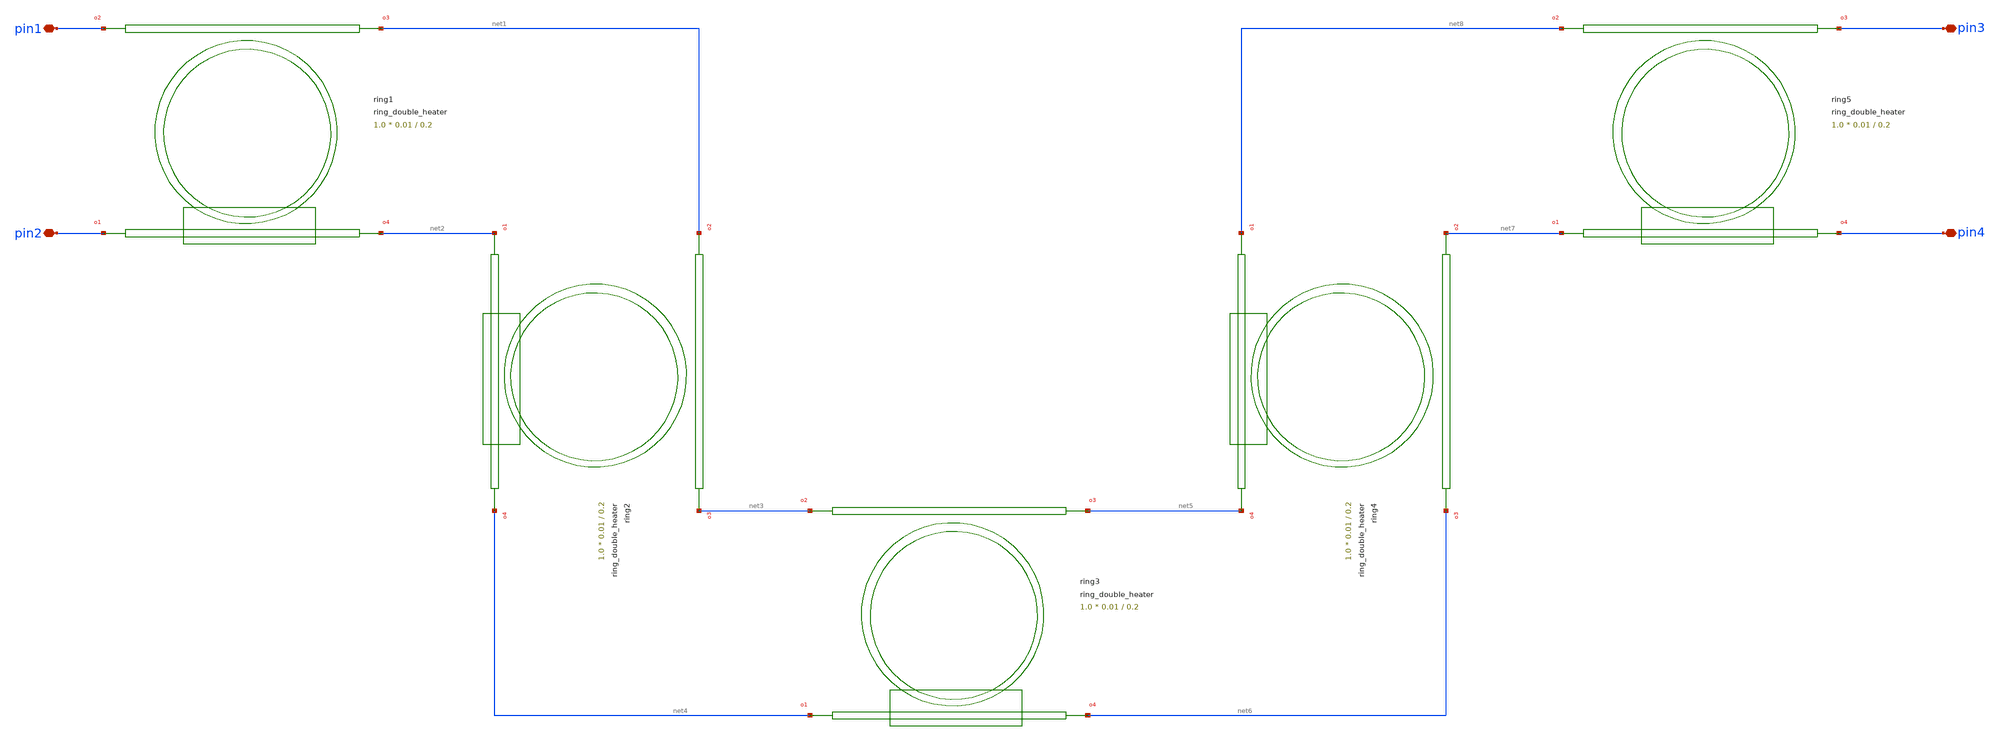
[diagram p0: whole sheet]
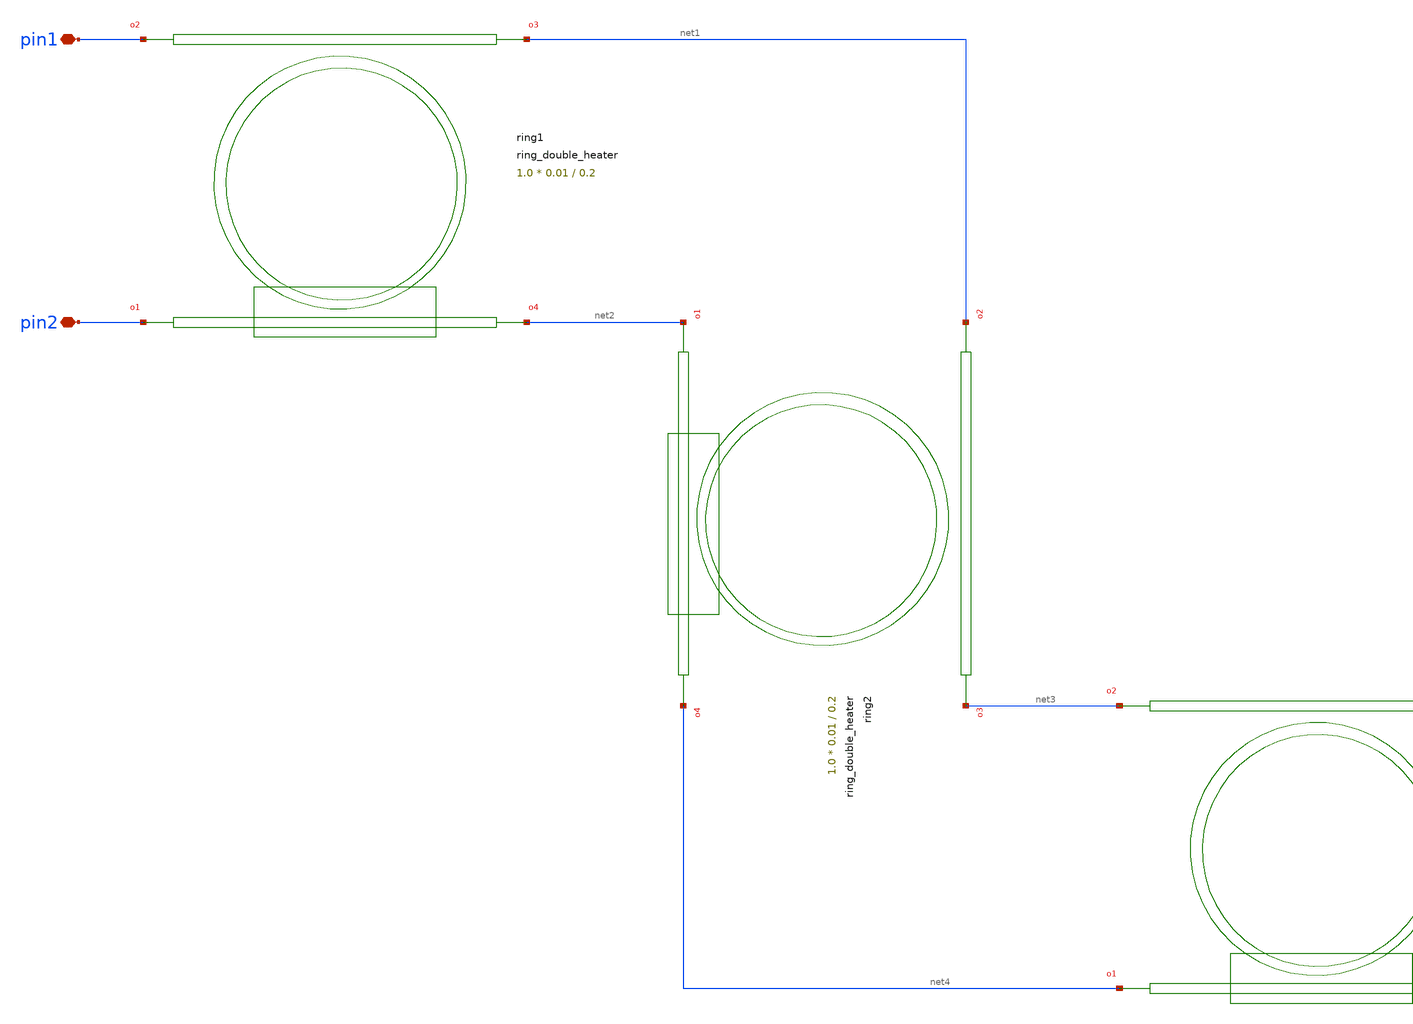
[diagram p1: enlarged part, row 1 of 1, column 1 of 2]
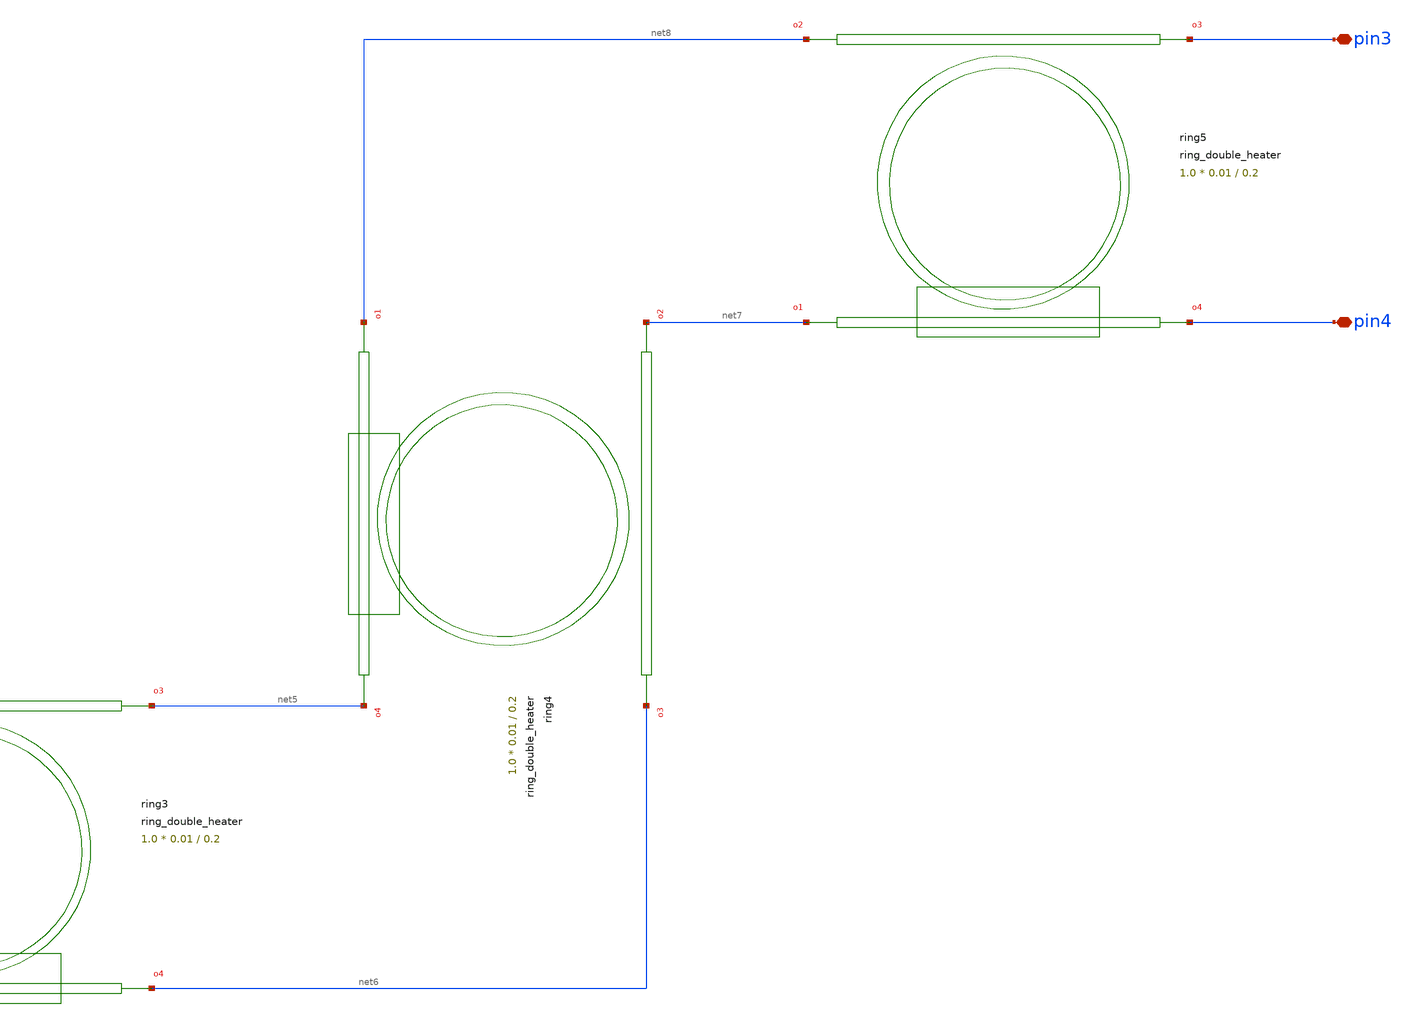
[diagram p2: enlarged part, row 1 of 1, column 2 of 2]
** sch_path: cells/xschem/tests/test_ring_double_heater.sch
* SPDX-FileCopyrightText: 2023 Mabrains Company
* Licensed under the GNU GENERAL PUBLIC License, Version 3.0 (the "License");
* you may not use this file except in compliance with the License.
* GNU GENERAL PUBLIC LICENSE
* Version 3, 29 June 2007
* This program is free software: you can redistribute it and/or modify
* it under the terms of the GNU General Public License as published
* by the Free Software Foundation, either 3 of the License, or
* (at your option) any later version.
* This program is distributed in the hope that it will be useful,
* but WITHOUT ANY WARRANTY; without even the implied warranty of
* MERCHANTABILITY or FITNESS FOR A PARTICULAR PURPOSE.  See the
* GNU General Public License for more details.
* You should have received a copy of the GNU General Public License
* along with this program.  If not, see <https://www.gnu.org/licenses/>.
* SPDX-License-Identifier: GPL-3.0
**.subckt test_ring_double_heater pin1 pin2 pin3 pin4
*.iopin pin1
*.iopin pin2
*.iopin pin3
*.iopin pin4
Pring1 pin2 pin1 net1 net2 ring_double_heater gap=0.2 gap_top=0.2 radius=10.0 length_x=1.0
+ length_y=0.01
Pring2 net2 net1 net3 net4 ring_double_heater gap=0.2 gap_top=0.2 radius=10.0 length_x=1.0
+ length_y=0.01
Pring3 net4 net3 net5 net6 ring_double_heater gap=0.2 gap_top=0.2 radius=10.0 length_x=1.0
+ length_y=0.01
Pring4 net8 net7 net6 net5 ring_double_heater gap=0.2 gap_top=0.2 radius=10.0 length_x=1.0
+ length_y=0.01
Pring5 net7 net8 pin3 pin4 ring_double_heater gap=0.2 gap_top=0.2 radius=10.0 length_x=1.0
+ length_y=0.01
**.ends
.end
